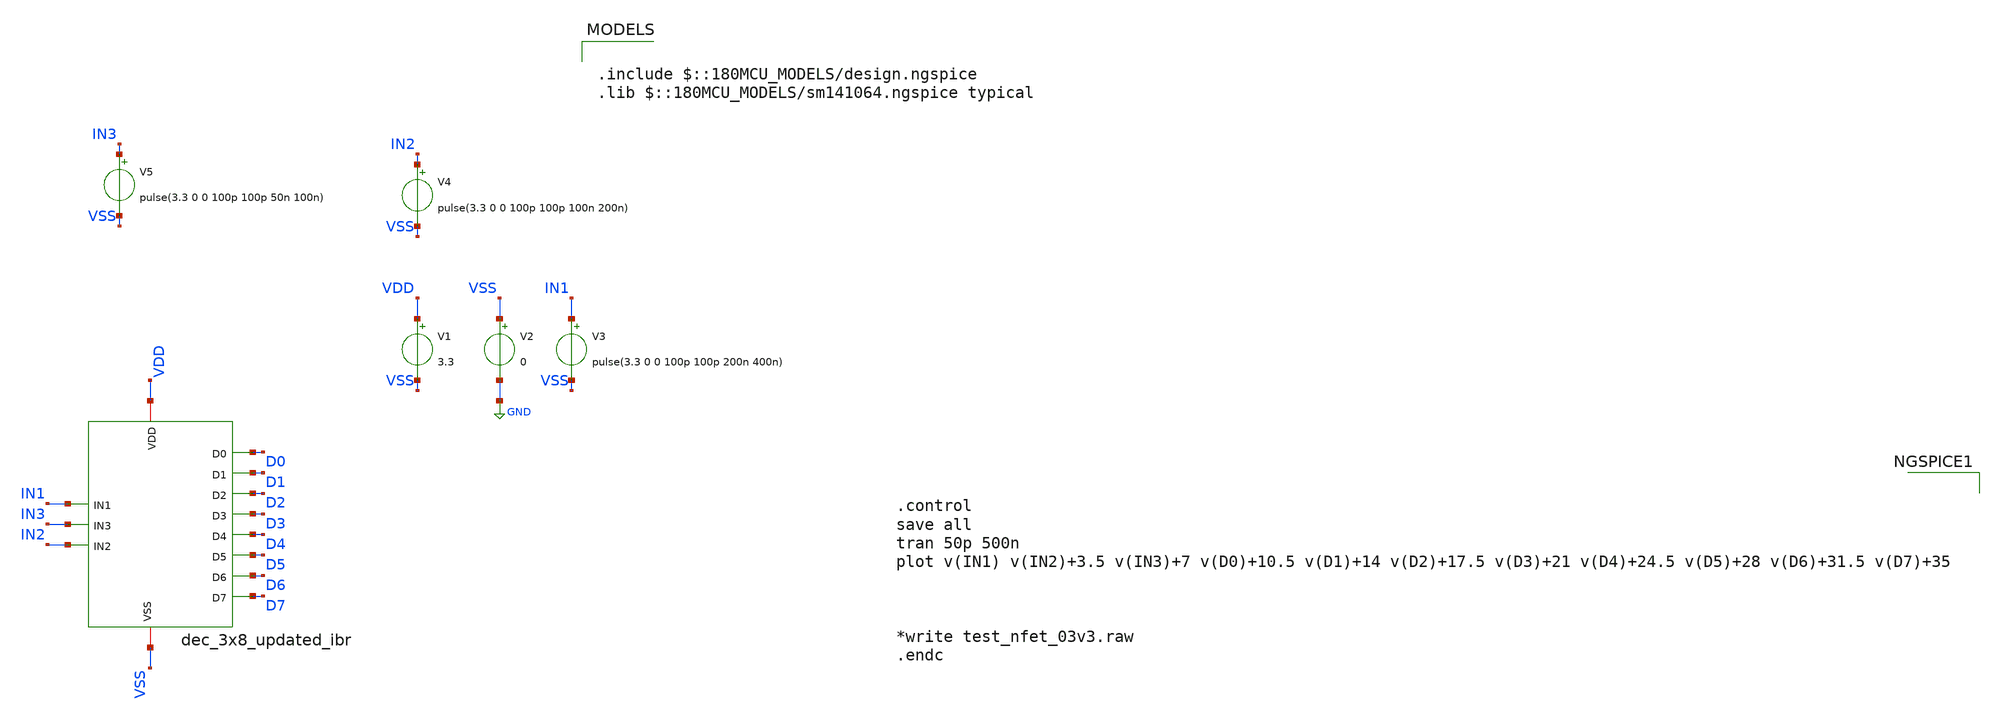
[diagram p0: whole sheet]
** sch_path: Clock_Generator_PAKISTAN_02/xschem/dec_3x8_test_updated_ibr.sch
**.subckt dec_3x8_test_updated_ibr
V1 VDD VSS 3.3
V2 VSS GND 0
V3 IN1 VSS pulse(3.3 0 0 100p 100p 200n 400n)
V4 IN2 VSS pulse(3.3 0 0 100p 100p 100n 200n)
V5 IN3 VSS pulse(3.3 0 0 100p 100p 50n 100n)
x1 IN1 VSS VDD D0 D1 D2 D3 D4 D5 D6 D7 IN3 IN2 dec_3x8_updated_ibr
**** begin user architecture code

.include $::180MCU_MODELS/design.ngspice
.lib $::180MCU_MODELS/sm141064.ngspice typical



.control
save all
tran 50p 500n
plot v(IN1) v(IN2)+3.5 v(IN3)+7 v(D0)+10.5 v(D1)+14 v(D2)+17.5 v(D3)+21 v(D4)+24.5 v(D5)+28
+ v(D6)+31.5 v(D7)+35



*write test_nfet_03v3.raw
.endc


**** end user architecture code
**.ends
.GLOBAL GND
.end
